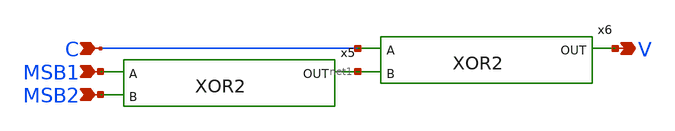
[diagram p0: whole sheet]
** sch_path: design/xschem/ZV_FLAG/V_FLAG.sch
**.subckt V_FLAG V C MSB1 MSB2
*.opin V
*.ipin C
*.ipin MSB1
*.ipin MSB2
x5 MSB1 MSB2 net1 XOR2
x6 C net1 V XOR2
**.ends

* expanding   symbol:  XOR/XOR2.sym # of pins=3
** sym_path: design/xschem/XOR/XOR2.sym
** sch_path: design/xschem/XOR/XOR2.sch
.subckt XOR2 A B OUT
*.ipin A
*.ipin B
*.opin OUT
x1 A B !B !A OUT !A A !B B VSS VDD cg4
x2 A VSS VDD !A inv
x3 B VSS VDD !B inv
.ends


* expanding   symbol:  ./CG4/cg4.sym # of pins=9
** sym_path: design/xschem/CG4/cg4.sym
** sch_path: design/xschem/CG4/cg4.sch
.subckt cg4 P3 P4 P2 P1 OUT N2 N1 N4 N3 VSS VDD
*.ipin P3
*.ipin P1
*.ipin N1
*.ipin N3
*.ipin P4
*.ipin P2
*.ipin N2
*.ipin N4
*.opin OUT
XM1 OUT N1 net1 VSS sky130_fd_pr__nfet_01v8 L=0.15 W=2 nf=1 ad='int((nf+1)/2) * W/nf * 0.29' as='int((nf+2)/2) * W/nf * 0.29'
+ pd='2*int((nf+1)/2) * (W/nf + 0.29)' ps='2*int((nf+2)/2) * (W/nf + 0.29)' nrd='0.29 / W' nrs='0.29 / W'
+ sa=0 sb=0 sd=0 mult=1 m=1
XM2 OUT N2 net2 VSS sky130_fd_pr__nfet_01v8 L=0.15 W=2 nf=1 ad='int((nf+1)/2) * W/nf * 0.29' as='int((nf+2)/2) * W/nf * 0.29'
+ pd='2*int((nf+1)/2) * (W/nf + 0.29)' ps='2*int((nf+2)/2) * (W/nf + 0.29)' nrd='0.29 / W' nrs='0.29 / W'
+ sa=0 sb=0 sd=0 mult=1 m=1
XM3 net1 N3 VSS VSS sky130_fd_pr__nfet_01v8 L=0.15 W=2 nf=1 ad='int((nf+1)/2) * W/nf * 0.29' as='int((nf+2)/2) * W/nf * 0.29'
+ pd='2*int((nf+1)/2) * (W/nf + 0.29)' ps='2*int((nf+2)/2) * (W/nf + 0.29)' nrd='0.29 / W' nrs='0.29 / W'
+ sa=0 sb=0 sd=0 mult=1 m=1
XM4 net2 N4 VSS VSS sky130_fd_pr__nfet_01v8 L=0.15 W=2 nf=1 ad='int((nf+1)/2) * W/nf * 0.29' as='int((nf+2)/2) * W/nf * 0.29'
+ pd='2*int((nf+1)/2) * (W/nf + 0.29)' ps='2*int((nf+2)/2) * (W/nf + 0.29)' nrd='0.29 / W' nrs='0.29 / W'
+ sa=0 sb=0 sd=0 mult=1 m=1
XM5 OUT P1 net3 VDD sky130_fd_pr__pfet_01v8 L=0.15 W=8.25 nf=1 ad='int((nf+1)/2) * W/nf * 0.29' as='int((nf+2)/2) * W/nf * 0.29'
+ pd='2*int((nf+1)/2) * (W/nf + 0.29)' ps='2*int((nf+2)/2) * (W/nf + 0.29)' nrd='0.29 / W' nrs='0.29 / W'
+ sa=0 sb=0 sd=0 mult=1 m=1
XM6 OUT P2 net3 VDD sky130_fd_pr__pfet_01v8 L=0.15 W=8.25 nf=1 ad='int((nf+1)/2) * W/nf * 0.29' as='int((nf+2)/2) * W/nf * 0.29'
+ pd='2*int((nf+1)/2) * (W/nf + 0.29)' ps='2*int((nf+2)/2) * (W/nf + 0.29)' nrd='0.29 / W' nrs='0.29 / W'
+ sa=0 sb=0 sd=0 mult=1 m=1
XM7 net3 P3 VDD VDD sky130_fd_pr__pfet_01v8 L=0.15 W=8.25 nf=1 ad='int((nf+1)/2) * W/nf * 0.29' as='int((nf+2)/2) * W/nf * 0.29'
+ pd='2*int((nf+1)/2) * (W/nf + 0.29)' ps='2*int((nf+2)/2) * (W/nf + 0.29)' nrd='0.29 / W' nrs='0.29 / W'
+ sa=0 sb=0 sd=0 mult=1 m=1
XM8 net3 P4 VDD VDD sky130_fd_pr__pfet_01v8 L=0.15 W=8.25 nf=1 ad='int((nf+1)/2) * W/nf * 0.29' as='int((nf+2)/2) * W/nf * 0.29'
+ pd='2*int((nf+1)/2) * (W/nf + 0.29)' ps='2*int((nf+2)/2) * (W/nf + 0.29)' nrd='0.29 / W' nrs='0.29 / W'
+ sa=0 sb=0 sd=0 mult=1 m=1
.ends


* expanding   symbol:  ./INV/inv.sym # of pins=2
** sym_path: design/xschem/INV/inv.sym
** sch_path: design/xschem/INV/inv.sch
.subckt inv A VSS VDD Y
*.ipin A
*.opin Y
XM2 Y A VSS GND sky130_fd_pr__nfet_01v8 L=0.15 W=1 nf=1 ad='int((nf+1)/2) * W/nf * 0.29' as='int((nf+2)/2) * W/nf * 0.29'
+ pd='2*int((nf+1)/2) * (W/nf + 0.29)' ps='2*int((nf+2)/2) * (W/nf + 0.29)' nrd='0.29 / W' nrs='0.29 / W'
+ sa=0 sb=0 sd=0 mult=1 m=1
XM1 Y A VDD VDD sky130_fd_pr__pfet_01v8 L=0.15 W=3.21 nf=1 ad='int((nf+1)/2) * W/nf * 0.29' as='int((nf+2)/2) * W/nf * 0.29'
+ pd='2*int((nf+1)/2) * (W/nf + 0.29)' ps='2*int((nf+2)/2) * (W/nf + 0.29)' nrd='0.29 / W' nrs='0.29 / W'
+ sa=0 sb=0 sd=0 mult=1 m=1
.ends

.end
